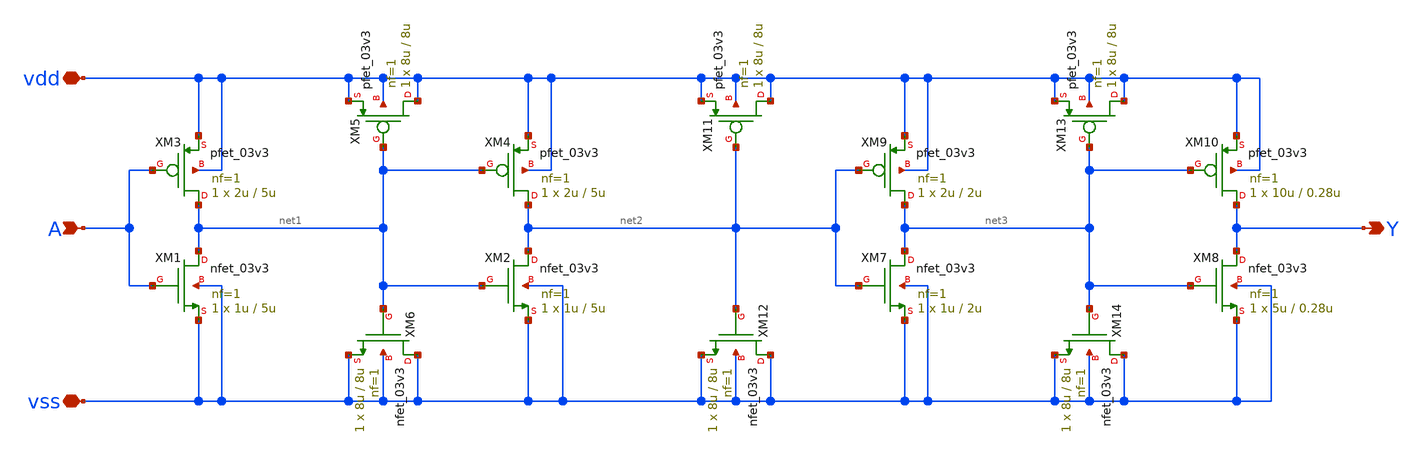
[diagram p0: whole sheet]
** sch_path: General/ADC/delay/delay.sch
**.subckt delay A Y vdd vss
*.ipin A
*.opin Y
*.iopin vdd
*.iopin vss
XM1 net1 A vss vss nfet_03v3 L=5u W=1u nf=1 ad='int((nf+1)/2) * W/nf * 0.18u' as='int((nf+2)/2) * W/nf * 0.18u'
+ pd='2*int((nf+1)/2) * (W/nf + 0.18u)' ps='2*int((nf+2)/2) * (W/nf + 0.18u)' nrd='0.18u / W' nrs='0.18u / W'
+ sa=0 sb=0 sd=0 m=1
XM3 net1 A vdd vdd pfet_03v3 L=5u W=2u nf=1 ad='int((nf+1)/2) * W/nf * 0.18u' as='int((nf+2)/2) * W/nf * 0.18u'
+ pd='2*int((nf+1)/2) * (W/nf + 0.18u)' ps='2*int((nf+2)/2) * (W/nf + 0.18u)' nrd='0.18u / W' nrs='0.18u / W'
+ sa=0 sb=0 sd=0 m=1
XM5 vdd net1 vdd vdd pfet_03v3 L=8u W=8u nf=1 ad='int((nf+1)/2) * W/nf * 0.18u' as='int((nf+2)/2) * W/nf * 0.18u'
+ pd='2*int((nf+1)/2) * (W/nf + 0.18u)' ps='2*int((nf+2)/2) * (W/nf + 0.18u)' nrd='0.18u / W' nrs='0.18u / W'
+ sa=0 sb=0 sd=0 m=1
XM6 vss net1 vss vss nfet_03v3 L=8u W=8u nf=1 ad='int((nf+1)/2) * W/nf * 0.18u' as='int((nf+2)/2) * W/nf * 0.18u'
+ pd='2*int((nf+1)/2) * (W/nf + 0.18u)' ps='2*int((nf+2)/2) * (W/nf + 0.18u)' nrd='0.18u / W' nrs='0.18u / W'
+ sa=0 sb=0 sd=0 m=1
XM7 net3 net2 vss vss nfet_03v3 L=2u W=1u nf=1 ad='int((nf+1)/2) * W/nf * 0.18u' as='int((nf+2)/2) * W/nf * 0.18u'
+ pd='2*int((nf+1)/2) * (W/nf + 0.18u)' ps='2*int((nf+2)/2) * (W/nf + 0.18u)' nrd='0.18u / W' nrs='0.18u / W'
+ sa=0 sb=0 sd=0 m=1
XM8 Y net3 vss vss nfet_03v3 L=0.28u W=5u nf=1 ad='int((nf+1)/2) * W/nf * 0.18u' as='int((nf+2)/2) * W/nf * 0.18u'
+ pd='2*int((nf+1)/2) * (W/nf + 0.18u)' ps='2*int((nf+2)/2) * (W/nf + 0.18u)' nrd='0.18u / W' nrs='0.18u / W'
+ sa=0 sb=0 sd=0 m=1
XM9 net3 net2 vdd vdd pfet_03v3 L=2u W=2u nf=1 ad='int((nf+1)/2) * W/nf * 0.18u' as='int((nf+2)/2) * W/nf * 0.18u'
+ pd='2*int((nf+1)/2) * (W/nf + 0.18u)' ps='2*int((nf+2)/2) * (W/nf + 0.18u)' nrd='0.18u / W' nrs='0.18u / W'
+ sa=0 sb=0 sd=0 m=1
XM10 Y net3 vdd vdd pfet_03v3 L=0.28u W=10u nf=1 ad='int((nf+1)/2) * W/nf * 0.18u' as='int((nf+2)/2) * W/nf * 0.18u'
+ pd='2*int((nf+1)/2) * (W/nf + 0.18u)' ps='2*int((nf+2)/2) * (W/nf + 0.18u)' nrd='0.18u / W' nrs='0.18u / W'
+ sa=0 sb=0 sd=0 m=1
XM11 vdd net2 vdd vdd pfet_03v3 L=8u W=8u nf=1 ad='int((nf+1)/2) * W/nf * 0.18u' as='int((nf+2)/2) * W/nf * 0.18u'
+ pd='2*int((nf+1)/2) * (W/nf + 0.18u)' ps='2*int((nf+2)/2) * (W/nf + 0.18u)' nrd='0.18u / W' nrs='0.18u / W'
+ sa=0 sb=0 sd=0 m=1
XM12 vss net2 vss vss nfet_03v3 L=8u W=8u nf=1 ad='int((nf+1)/2) * W/nf * 0.18u' as='int((nf+2)/2) * W/nf * 0.18u'
+ pd='2*int((nf+1)/2) * (W/nf + 0.18u)' ps='2*int((nf+2)/2) * (W/nf + 0.18u)' nrd='0.18u / W' nrs='0.18u / W'
+ sa=0 sb=0 sd=0 m=1
XM13 vdd net3 vdd vdd pfet_03v3 L=8u W=8u nf=1 ad='int((nf+1)/2) * W/nf * 0.18u' as='int((nf+2)/2) * W/nf * 0.18u'
+ pd='2*int((nf+1)/2) * (W/nf + 0.18u)' ps='2*int((nf+2)/2) * (W/nf + 0.18u)' nrd='0.18u / W' nrs='0.18u / W'
+ sa=0 sb=0 sd=0 m=1
XM14 vss net3 vss vss nfet_03v3 L=8u W=8u nf=1 ad='int((nf+1)/2) * W/nf * 0.18u' as='int((nf+2)/2) * W/nf * 0.18u'
+ pd='2*int((nf+1)/2) * (W/nf + 0.18u)' ps='2*int((nf+2)/2) * (W/nf + 0.18u)' nrd='0.18u / W' nrs='0.18u / W'
+ sa=0 sb=0 sd=0 m=1
XM2 net2 net1 vss vss nfet_03v3 L=5u W=1u nf=1 ad='int((nf+1)/2) * W/nf * 0.18u' as='int((nf+2)/2) * W/nf * 0.18u'
+ pd='2*int((nf+1)/2) * (W/nf + 0.18u)' ps='2*int((nf+2)/2) * (W/nf + 0.18u)' nrd='0.18u / W' nrs='0.18u / W'
+ sa=0 sb=0 sd=0 m=1
XM4 net2 net1 vdd vdd pfet_03v3 L=5u W=2u nf=1 ad='int((nf+1)/2) * W/nf * 0.18u' as='int((nf+2)/2) * W/nf * 0.18u'
+ pd='2*int((nf+1)/2) * (W/nf + 0.18u)' ps='2*int((nf+2)/2) * (W/nf + 0.18u)' nrd='0.18u / W' nrs='0.18u / W'
+ sa=0 sb=0 sd=0 m=1
**.ends
.end
